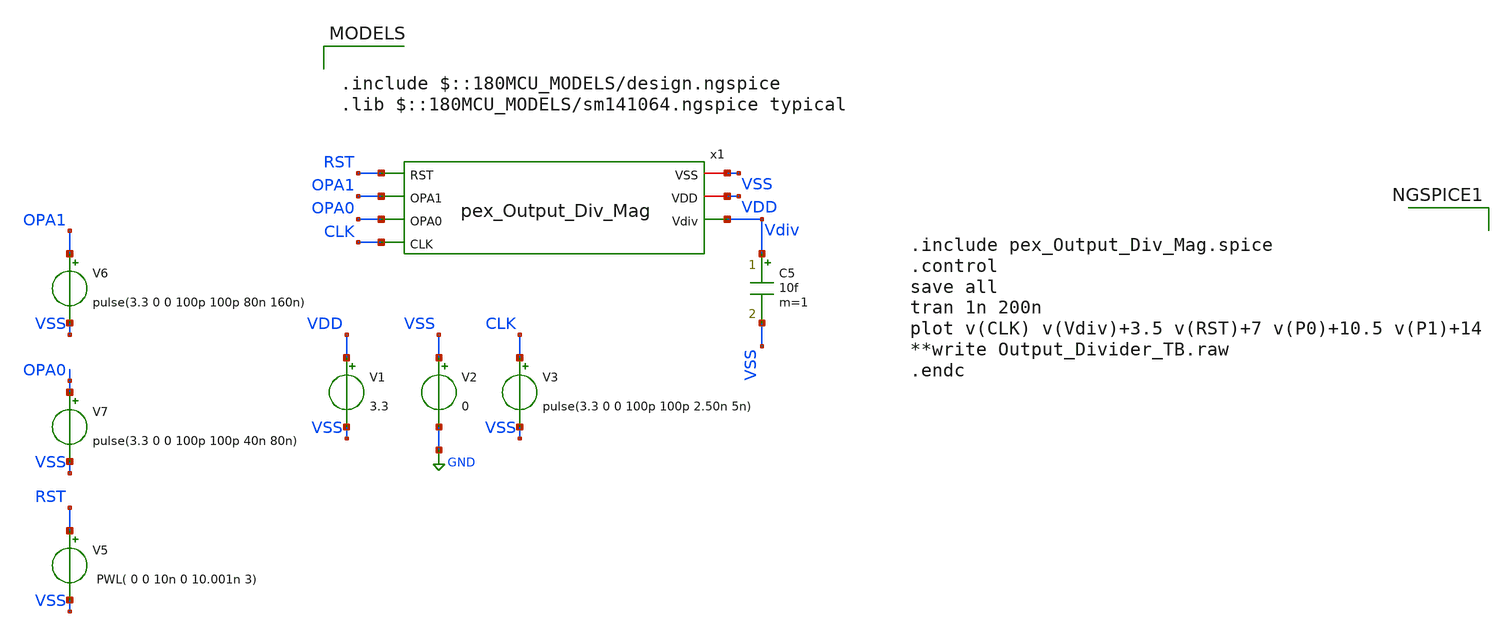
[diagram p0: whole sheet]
** sch_path: Clock_Generator_PAKISTAN_02/Schematics/pex_output_divider_tb.sch
**.subckt pex_output_divider_tb
V1 VDD VSS 3.3
V2 VSS GND 0
V3 CLK VSS pulse(3.3 0 0 100p 100p 2.50n 5n)
C5 Vdiv VSS 10f m=1
V5 RST VSS PWL( 0 0 10n 0 10.001n 3)
V6 OPA1 VSS pulse(3.3 0 0 100p 100p 80n 160n)
V7 OPA0 VSS pulse(3.3 0 0 100p 100p 40n 80n)
x1 VSS VDD RST Vdiv OPA1 OPA0 CLK pex_Output_Div_Mag
**** begin user architecture code

.include $::180MCU_MODELS/design.ngspice
.lib $::180MCU_MODELS/sm141064.ngspice typical



.include pex_Output_Div_Mag.spice
.control
save all
tran 1n 200n
plot v(CLK) v(Vdiv)+3.5 v(RST)+7 v(P0)+10.5 v(P1)+14
**write Output_Divider_TB.raw
.endc


**** end user architecture code
**.ends
.GLOBAL GND
.end
